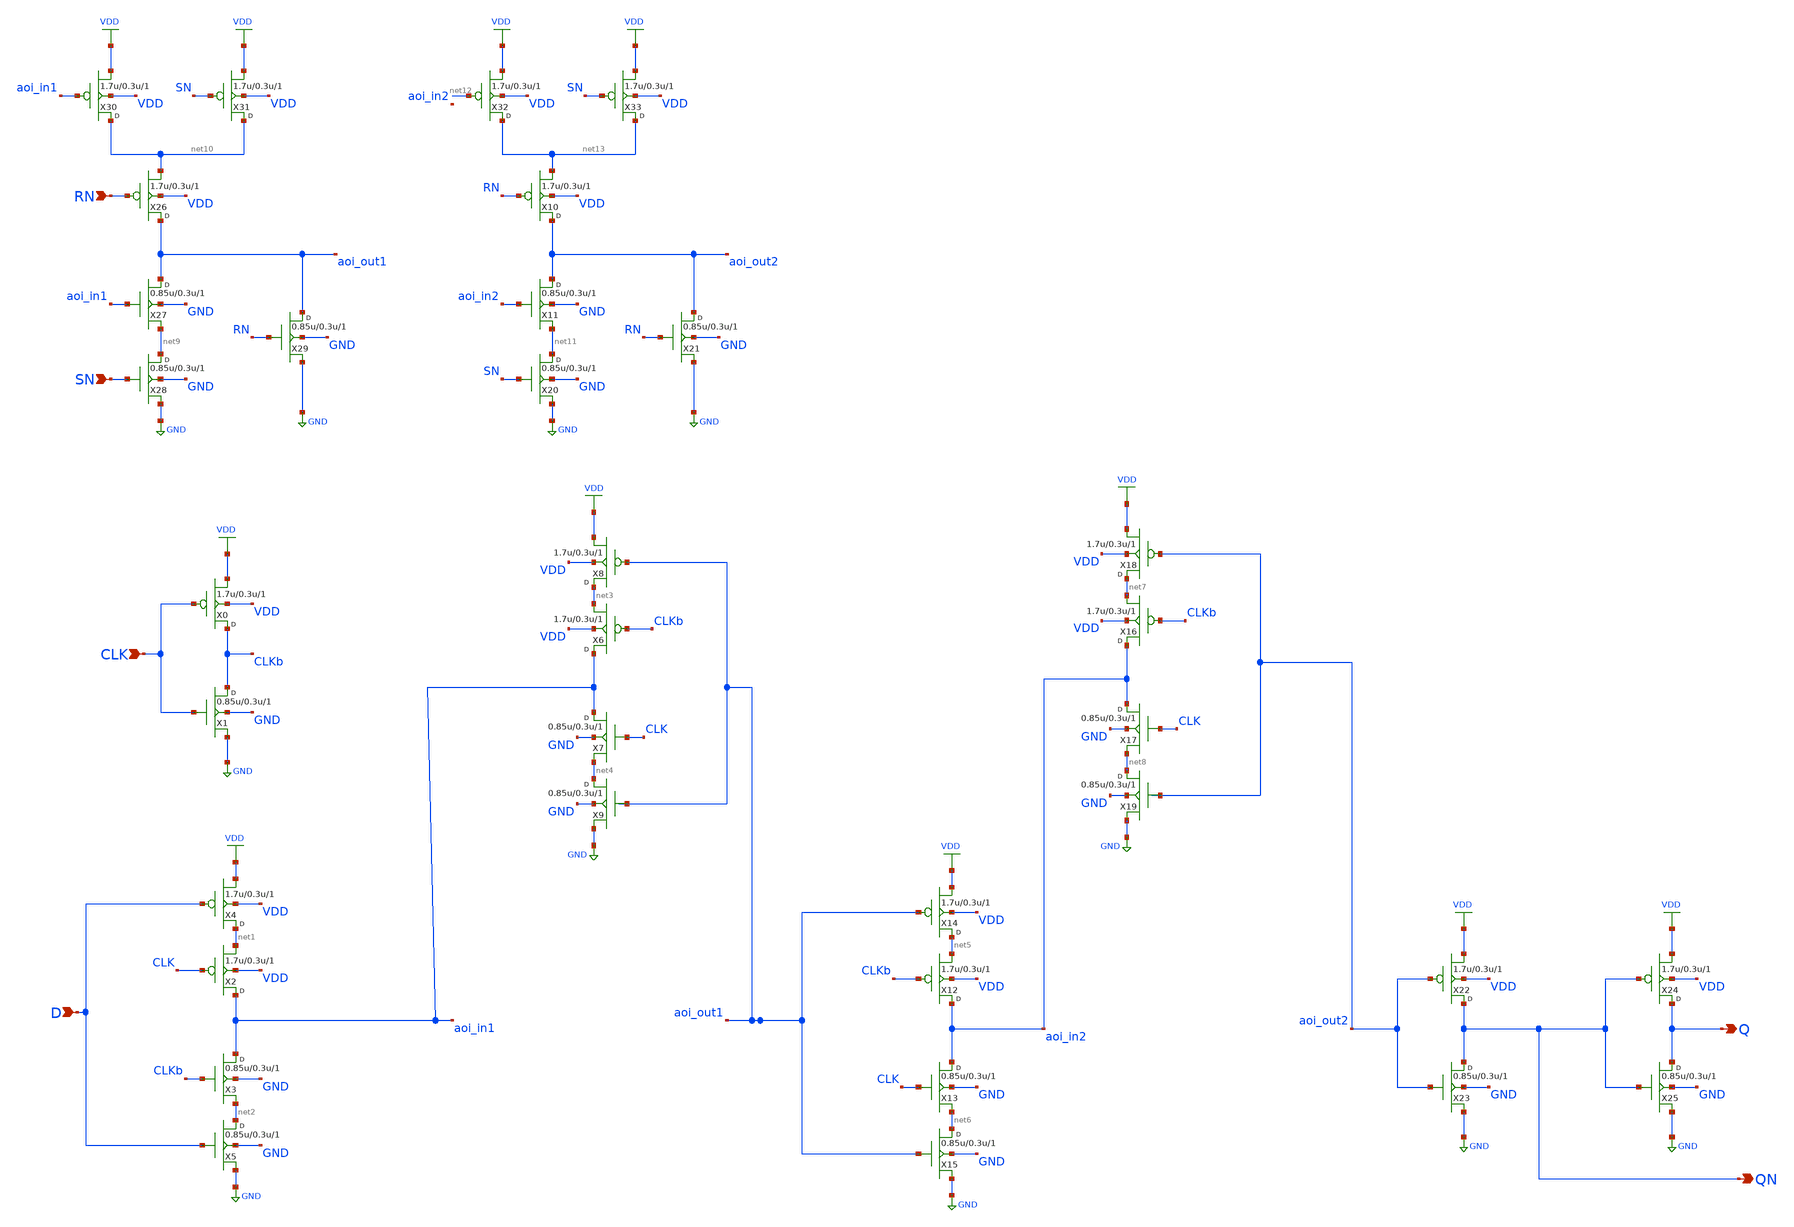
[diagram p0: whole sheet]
** sch_path: lib/12T/schematics/gf180mcu_osu_sc_dffsr_1.sch
**.subckt gf180mcu_osu_sc_dffsr_1 CLK D Q QN SN RN
*.ipin CLK
*.ipin D
*.opin Q
*.opin QN
*.ipin SN
*.ipin RN
X0 CLKb CLK VDD VDD pmos_3p3 w=1.7u l=0.3u m=1
X1 CLKb CLK GND GND nmos_3p3 w=0.85u l=0.3u m=1
X2 aoi_in1 CLK net1 VDD pmos_3p3 w=1.7u l=0.3u m=1
X3 aoi_in1 CLKb net2 GND nmos_3p3 w=0.85u l=0.3u m=1
X4 net1 D VDD VDD pmos_3p3 w=1.7u l=0.3u m=1
X5 net2 D GND GND nmos_3p3 w=0.85u l=0.3u m=1
X6 aoi_in1 CLKb net3 VDD pmos_3p3 w=1.7u l=0.3u m=1
X7 aoi_in1 CLK net4 GND nmos_3p3 w=0.85u l=0.3u m=1
X8 net3 aoi_out1 VDD VDD pmos_3p3 w=1.7u l=0.3u m=1
X9 net4 aoi_out1 GND GND nmos_3p3 w=0.85u l=0.3u m=1
X12 aoi_in2 CLKb net5 VDD pmos_3p3 w=1.7u l=0.3u m=1
X13 aoi_in2 CLK net6 GND nmos_3p3 w=0.85u l=0.3u m=1
X14 net5 aoi_out1 VDD VDD pmos_3p3 w=1.7u l=0.3u m=1
X15 net6 aoi_out1 GND GND nmos_3p3 w=0.85u l=0.3u m=1
X16 aoi_in2 CLKb net7 VDD pmos_3p3 w=1.7u l=0.3u m=1
X17 aoi_in2 CLK net8 GND nmos_3p3 w=0.85u l=0.3u m=1
X18 net7 aoi_out2 VDD VDD pmos_3p3 w=1.7u l=0.3u m=1
X19 net8 aoi_out2 GND GND nmos_3p3 w=0.85u l=0.3u m=1
X22 QN aoi_out2 VDD VDD pmos_3p3 w=1.7u l=0.3u m=1
X23 QN aoi_out2 GND GND nmos_3p3 w=0.85u l=0.3u m=1
X24 Q QN VDD VDD pmos_3p3 w=1.7u l=0.3u m=1
X25 Q QN GND GND nmos_3p3 w=0.85u l=0.3u m=1
X26 aoi_out1 RN net10 VDD pmos_3p3 w=1.7u l=0.3u m=1
X27 aoi_out1 aoi_in1 net9 GND nmos_3p3 w=0.85u l=0.3u m=1
X28 net9 SN GND GND nmos_3p3 w=0.85u l=0.3u m=1
X29 aoi_out1 RN GND GND nmos_3p3 w=0.85u l=0.3u m=1
X30 net10 aoi_in1 VDD VDD pmos_3p3 w=1.7u l=0.3u m=1
X31 net10 SN VDD VDD pmos_3p3 w=1.7u l=0.3u m=1
X10 aoi_out2 RN net13 VDD pmos_3p3 w=1.7u l=0.3u m=1
X11 aoi_out2 aoi_in2 net11 GND nmos_3p3 w=0.85u l=0.3u m=1
X20 net11 SN GND GND nmos_3p3 w=0.85u l=0.3u m=1
X21 aoi_out2 RN GND GND nmos_3p3 w=0.85u l=0.3u m=1
X32 net13 net12 VDD VDD pmos_3p3 w=1.7u l=0.3u m=1
X33 net13 SN VDD VDD pmos_3p3 w=1.7u l=0.3u m=1
**** begin user architecture code


.inc "/import/yukari1/lrburle/OSU_180/char/techfiles/design.hspice"
.lib "/import/yukari1/lrburle/OSU_180/char/techfiles/sm141064.hspice" typical


**** end user architecture code
**.ends
.GLOBAL VDD
.GLOBAL GND
.end
